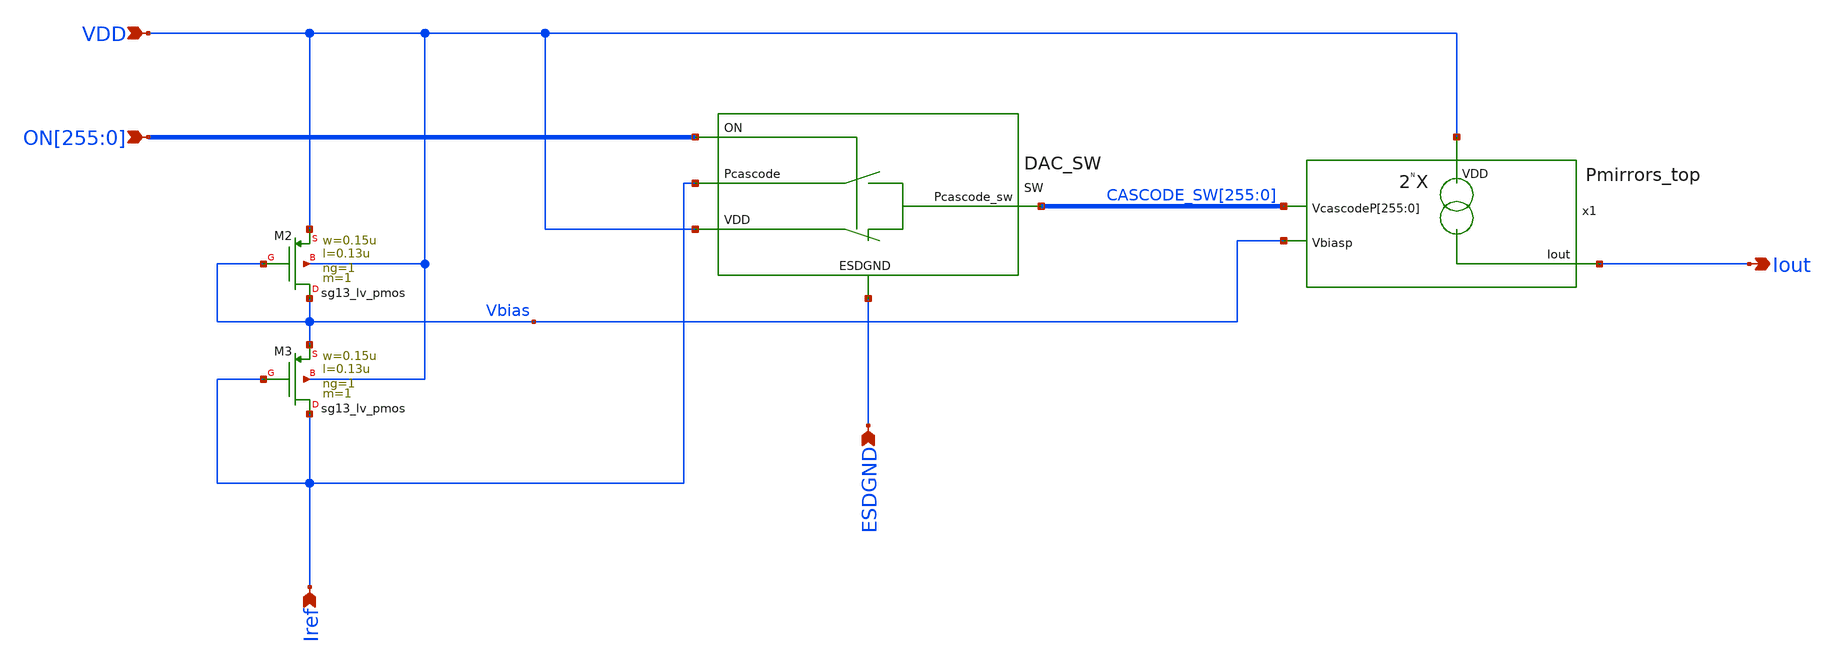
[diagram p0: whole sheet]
** sch_path: xschem/DAC_TOP.sch
**.subckt DAC_TOP VDD Iout ESDGND
*+ ON[255],ON[254],ON[253],ON[252],ON[251],ON[250],ON[249],ON[248],ON[247],ON[246],ON[245],ON[244],ON[243],ON[242],ON[241],ON[240],ON[239],ON[238],ON[237],ON[236],ON[235],ON[234],ON[233],ON[232],ON[231],ON[230],ON[229],ON[228],ON[227],ON[226],ON[225],ON[224],ON[223],ON[222],ON[221],ON[220],ON[219],ON[218],ON[217],ON[216],ON[215],ON[214],ON[213],ON[212],ON[211],ON[210],ON[209],ON[208],ON[207],ON[206],ON[205],ON[204],ON[203],ON[202],ON[201],ON[200],ON[199],ON[198],ON[197],ON[196],ON[195],ON[194],ON[193],ON[192],ON[191],ON[190],ON[189],ON[188],ON[187],ON[186],ON[185],ON[184],ON[183],ON[182],ON[181],ON[180],ON[179],ON[178],ON[177],ON[176],ON[175],ON[174],ON[173],ON[172],ON[171],ON[170],ON[169],ON[168],ON[167],ON[166],ON[165],ON[164],ON[163],ON[162],ON[161],ON[160],ON[159],ON[158],ON[157],ON[156],ON[155],ON[154],ON[153],ON[152],ON[151],ON[150],ON[149],ON[148],ON[147],ON[146],ON[145],ON[144],ON[143],ON[142],ON[141],ON[140],ON[139],ON[138],ON[137],ON[136],ON[135],ON[134],ON[133],ON[132],ON[131],ON[130],ON[129],ON[128],ON[127],ON[126],ON[125],ON[124],ON[123],ON[122],ON[121],ON[120],ON[119],ON[118],ON[117],ON[116],ON[115],ON[114],ON[113],ON[112],ON[111],ON[110],ON[109],ON[108],ON[107],ON[106],ON[105],ON[104],ON[103],ON[102],ON[101],ON[100],ON[99],ON[98],ON[97],ON[96],ON[95],ON[94],ON[93],ON[92],ON[91],ON[90],ON[89],ON[88],ON[87],ON[86],ON[85],ON[84],ON[83],ON[82],ON[81],ON[80],ON[79],ON[78],ON[77],ON[76],ON[75],ON[74],ON[73],ON[72],ON[71],ON[70],ON[69],ON[68],ON[67],ON[66],ON[65],ON[64],ON[63],ON[62],ON[61],ON[60],ON[59],ON[58],ON[57],ON[56],ON[55],ON[54],ON[53],ON[52],ON[51],ON[50],ON[49],ON[48],ON[47],ON[46],ON[45],ON[44],ON[43],ON[42],ON[41],ON[40],ON[39],ON[38],ON[37],ON[36],ON[35],ON[34],ON[33],ON[32],ON[31],ON[30],ON[29],ON[28],ON[27],ON[26],ON[25],ON[24],ON[23],ON[22],ON[21],ON[20],ON[19],ON[18],ON[17],ON[16],ON[15],ON[14],ON[13],ON[12],ON[11],ON[10],ON[9],ON[8],ON[7],ON[6],ON[5],ON[4],ON[3],ON[2],ON[1],ON[0] Iref
*.ipin VDD
*.opin Iout
*.ipin ESDGND
*.ipin
*+ ON[255],ON[254],ON[253],ON[252],ON[251],ON[250],ON[249],ON[248],ON[247],ON[246],ON[245],ON[244],ON[243],ON[242],ON[241],ON[240],ON[239],ON[238],ON[237],ON[236],ON[235],ON[234],ON[233],ON[232],ON[231],ON[230],ON[229],ON[228],ON[227],ON[226],ON[225],ON[224],ON[223],ON[222],ON[221],ON[220],ON[219],ON[218],ON[217],ON[216],ON[215],ON[214],ON[213],ON[212],ON[211],ON[210],ON[209],ON[208],ON[207],ON[206],ON[205],ON[204],ON[203],ON[202],ON[201],ON[200],ON[199],ON[198],ON[197],ON[196],ON[195],ON[194],ON[193],ON[192],ON[191],ON[190],ON[189],ON[188],ON[187],ON[186],ON[185],ON[184],ON[183],ON[182],ON[181],ON[180],ON[179],ON[178],ON[177],ON[176],ON[175],ON[174],ON[173],ON[172],ON[171],ON[170],ON[169],ON[168],ON[167],ON[166],ON[165],ON[164],ON[163],ON[162],ON[161],ON[160],ON[159],ON[158],ON[157],ON[156],ON[155],ON[154],ON[153],ON[152],ON[151],ON[150],ON[149],ON[148],ON[147],ON[146],ON[145],ON[144],ON[143],ON[142],ON[141],ON[140],ON[139],ON[138],ON[137],ON[136],ON[135],ON[134],ON[133],ON[132],ON[131],ON[130],ON[129],ON[128],ON[127],ON[126],ON[125],ON[124],ON[123],ON[122],ON[121],ON[120],ON[119],ON[118],ON[117],ON[116],ON[115],ON[114],ON[113],ON[112],ON[111],ON[110],ON[109],ON[108],ON[107],ON[106],ON[105],ON[104],ON[103],ON[102],ON[101],ON[100],ON[99],ON[98],ON[97],ON[96],ON[95],ON[94],ON[93],ON[92],ON[91],ON[90],ON[89],ON[88],ON[87],ON[86],ON[85],ON[84],ON[83],ON[82],ON[81],ON[80],ON[79],ON[78],ON[77],ON[76],ON[75],ON[74],ON[73],ON[72],ON[71],ON[70],ON[69],ON[68],ON[67],ON[66],ON[65],ON[64],ON[63],ON[62],ON[61],ON[60],ON[59],ON[58],ON[57],ON[56],ON[55],ON[54],ON[53],ON[52],ON[51],ON[50],ON[49],ON[48],ON[47],ON[46],ON[45],ON[44],ON[43],ON[42],ON[41],ON[40],ON[39],ON[38],ON[37],ON[36],ON[35],ON[34],ON[33],ON[32],ON[31],ON[30],ON[29],ON[28],ON[27],ON[26],ON[25],ON[24],ON[23],ON[22],ON[21],ON[20],ON[19],ON[18],ON[17],ON[16],ON[15],ON[14],ON[13],ON[12],ON[11],ON[10],ON[9],ON[8],ON[7],ON[6],ON[5],ON[4],ON[3],ON[2],ON[1],ON[0]
*.ipin Iref
x1 VDD Iout Vbias CASCODE_SW[255] CASCODE_SW[254] CASCODE_SW[253] CASCODE_SW[252] CASCODE_SW[251]
+ CASCODE_SW[250] CASCODE_SW[249] CASCODE_SW[248] CASCODE_SW[247] CASCODE_SW[246] CASCODE_SW[245] CASCODE_SW[244]
+ CASCODE_SW[243] CASCODE_SW[242] CASCODE_SW[241] CASCODE_SW[240] CASCODE_SW[239] CASCODE_SW[238] CASCODE_SW[237]
+ CASCODE_SW[236] CASCODE_SW[235] CASCODE_SW[234] CASCODE_SW[233] CASCODE_SW[232] CASCODE_SW[231] CASCODE_SW[230]
+ CASCODE_SW[229] CASCODE_SW[228] CASCODE_SW[227] CASCODE_SW[226] CASCODE_SW[225] CASCODE_SW[224] CASCODE_SW[223]
+ CASCODE_SW[222] CASCODE_SW[221] CASCODE_SW[220] CASCODE_SW[219] CASCODE_SW[218] CASCODE_SW[217] CASCODE_SW[216]
+ CASCODE_SW[215] CASCODE_SW[214] CASCODE_SW[213] CASCODE_SW[212] CASCODE_SW[211] CASCODE_SW[210] CASCODE_SW[209]
+ CASCODE_SW[208] CASCODE_SW[207] CASCODE_SW[206] CASCODE_SW[205] CASCODE_SW[204] CASCODE_SW[203] CASCODE_SW[202]
+ CASCODE_SW[201] CASCODE_SW[200] CASCODE_SW[199] CASCODE_SW[198] CASCODE_SW[197] CASCODE_SW[196] CASCODE_SW[195]
+ CASCODE_SW[194] CASCODE_SW[193] CASCODE_SW[192] CASCODE_SW[191] CASCODE_SW[190] CASCODE_SW[189] CASCODE_SW[188]
+ CASCODE_SW[187] CASCODE_SW[186] CASCODE_SW[185] CASCODE_SW[184] CASCODE_SW[183] CASCODE_SW[182] CASCODE_SW[181]
+ CASCODE_SW[180] CASCODE_SW[179] CASCODE_SW[178] CASCODE_SW[177] CASCODE_SW[176] CASCODE_SW[175] CASCODE_SW[174]
+ CASCODE_SW[173] CASCODE_SW[172] CASCODE_SW[171] CASCODE_SW[170] CASCODE_SW[169] CASCODE_SW[168] CASCODE_SW[167]
+ CASCODE_SW[166] CASCODE_SW[165] CASCODE_SW[164] CASCODE_SW[163] CASCODE_SW[162] CASCODE_SW[161] CASCODE_SW[160]
+ CASCODE_SW[159] CASCODE_SW[158] CASCODE_SW[157] CASCODE_SW[156] CASCODE_SW[155] CASCODE_SW[154] CASCODE_SW[153]
+ CASCODE_SW[152] CASCODE_SW[151] CASCODE_SW[150] CASCODE_SW[149] CASCODE_SW[148] CASCODE_SW[147] CASCODE_SW[146]
+ CASCODE_SW[145] CASCODE_SW[144] CASCODE_SW[143] CASCODE_SW[142] CASCODE_SW[141] CASCODE_SW[140] CASCODE_SW[139]
+ CASCODE_SW[138] CASCODE_SW[137] CASCODE_SW[136] CASCODE_SW[135] CASCODE_SW[134] CASCODE_SW[133] CASCODE_SW[132]
+ CASCODE_SW[131] CASCODE_SW[130] CASCODE_SW[129] CASCODE_SW[128] CASCODE_SW[127] CASCODE_SW[126] CASCODE_SW[125]
+ CASCODE_SW[124] CASCODE_SW[123] CASCODE_SW[122] CASCODE_SW[121] CASCODE_SW[120] CASCODE_SW[119] CASCODE_SW[118]
+ CASCODE_SW[117] CASCODE_SW[116] CASCODE_SW[115] CASCODE_SW[114] CASCODE_SW[113] CASCODE_SW[112] CASCODE_SW[111]
+ CASCODE_SW[110] CASCODE_SW[109] CASCODE_SW[108] CASCODE_SW[107] CASCODE_SW[106] CASCODE_SW[105] CASCODE_SW[104]
+ CASCODE_SW[103] CASCODE_SW[102] CASCODE_SW[101] CASCODE_SW[100] CASCODE_SW[99] CASCODE_SW[98] CASCODE_SW[97]
+ CASCODE_SW[96] CASCODE_SW[95] CASCODE_SW[94] CASCODE_SW[93] CASCODE_SW[92] CASCODE_SW[91] CASCODE_SW[90]
+ CASCODE_SW[89] CASCODE_SW[88] CASCODE_SW[87] CASCODE_SW[86] CASCODE_SW[85] CASCODE_SW[84] CASCODE_SW[83]
+ CASCODE_SW[82] CASCODE_SW[81] CASCODE_SW[80] CASCODE_SW[79] CASCODE_SW[78] CASCODE_SW[77] CASCODE_SW[76]
+ CASCODE_SW[75] CASCODE_SW[74] CASCODE_SW[73] CASCODE_SW[72] CASCODE_SW[71] CASCODE_SW[70] CASCODE_SW[69]
+ CASCODE_SW[68] CASCODE_SW[67] CASCODE_SW[66] CASCODE_SW[65] CASCODE_SW[64] CASCODE_SW[63] CASCODE_SW[62]
+ CASCODE_SW[61] CASCODE_SW[60] CASCODE_SW[59] CASCODE_SW[58] CASCODE_SW[57] CASCODE_SW[56] CASCODE_SW[55]
+ CASCODE_SW[54] CASCODE_SW[53] CASCODE_SW[52] CASCODE_SW[51] CASCODE_SW[50] CASCODE_SW[49] CASCODE_SW[48]
+ CASCODE_SW[47] CASCODE_SW[46] CASCODE_SW[45] CASCODE_SW[44] CASCODE_SW[43] CASCODE_SW[42] CASCODE_SW[41]
+ CASCODE_SW[40] CASCODE_SW[39] CASCODE_SW[38] CASCODE_SW[37] CASCODE_SW[36] CASCODE_SW[35] CASCODE_SW[34]
+ CASCODE_SW[33] CASCODE_SW[32] CASCODE_SW[31] CASCODE_SW[30] CASCODE_SW[29] CASCODE_SW[28] CASCODE_SW[27]
+ CASCODE_SW[26] CASCODE_SW[25] CASCODE_SW[24] CASCODE_SW[23] CASCODE_SW[22] CASCODE_SW[21] CASCODE_SW[20]
+ CASCODE_SW[19] CASCODE_SW[18] CASCODE_SW[17] CASCODE_SW[16] CASCODE_SW[15] CASCODE_SW[14] CASCODE_SW[13]
+ CASCODE_SW[12] CASCODE_SW[11] CASCODE_SW[10] CASCODE_SW[9] CASCODE_SW[8] CASCODE_SW[7] CASCODE_SW[6] CASCODE_SW[5]
+ CASCODE_SW[4] CASCODE_SW[3] CASCODE_SW[2] CASCODE_SW[1] CASCODE_SW[0] Pmirrors_top
SW VDD ON[255] CASCODE_SW[255] Iref ESDGND DAC_SW
XM2 Vbias Vbias VDD VDD sg13_lv_pmos w=0.15u l=0.13u ng=1 m=1 mm_ok=1
XM3 Iref Iref Vbias VDD sg13_lv_pmos w=0.15u l=0.13u ng=1 m=1 mm_ok=1
**.ends

* expanding   symbol:  /home/user/PUDDING/schematic/Pmirrors_top.sym # of pins=4
** sym_path: /home/user/PUDDING/schematic/Pmirrors_top.sym
** sch_path: /home/user/PUDDING/schematic/Pmirrors_top.sch
.subckt Pmirrors_top VDD Iout Vbiasp VcascodeP[255] VcascodeP[254] VcascodeP[253] VcascodeP[252]
+ VcascodeP[251] VcascodeP[250] VcascodeP[249] VcascodeP[248] VcascodeP[247] VcascodeP[246] VcascodeP[245]
+ VcascodeP[244] VcascodeP[243] VcascodeP[242] VcascodeP[241] VcascodeP[240] VcascodeP[239] VcascodeP[238]
+ VcascodeP[237] VcascodeP[236] VcascodeP[235] VcascodeP[234] VcascodeP[233] VcascodeP[232] VcascodeP[231]
+ VcascodeP[230] VcascodeP[229] VcascodeP[228] VcascodeP[227] VcascodeP[226] VcascodeP[225] VcascodeP[224]
+ VcascodeP[223] VcascodeP[222] VcascodeP[221] VcascodeP[220] VcascodeP[219] VcascodeP[218] VcascodeP[217]
+ VcascodeP[216] VcascodeP[215] VcascodeP[214] VcascodeP[213] VcascodeP[212] VcascodeP[211] VcascodeP[210]
+ VcascodeP[209] VcascodeP[208] VcascodeP[207] VcascodeP[206] VcascodeP[205] VcascodeP[204] VcascodeP[203]
+ VcascodeP[202] VcascodeP[201] VcascodeP[200] VcascodeP[199] VcascodeP[198] VcascodeP[197] VcascodeP[196]
+ VcascodeP[195] VcascodeP[194] VcascodeP[193] VcascodeP[192] VcascodeP[191] VcascodeP[190] VcascodeP[189]
+ VcascodeP[188] VcascodeP[187] VcascodeP[186] VcascodeP[185] VcascodeP[184] VcascodeP[183] VcascodeP[182]
+ VcascodeP[181] VcascodeP[180] VcascodeP[179] VcascodeP[178] VcascodeP[177] VcascodeP[176] VcascodeP[175]
+ VcascodeP[174] VcascodeP[173] VcascodeP[172] VcascodeP[171] VcascodeP[170] VcascodeP[169] VcascodeP[168]
+ VcascodeP[167] VcascodeP[166] VcascodeP[165] VcascodeP[164] VcascodeP[163] VcascodeP[162] VcascodeP[161]
+ VcascodeP[160] VcascodeP[159] VcascodeP[158] VcascodeP[157] VcascodeP[156] VcascodeP[155] VcascodeP[154]
+ VcascodeP[153] VcascodeP[152] VcascodeP[151] VcascodeP[150] VcascodeP[149] VcascodeP[148] VcascodeP[147]
+ VcascodeP[146] VcascodeP[145] VcascodeP[144] VcascodeP[143] VcascodeP[142] VcascodeP[141] VcascodeP[140]
+ VcascodeP[139] VcascodeP[138] VcascodeP[137] VcascodeP[136] VcascodeP[135] VcascodeP[134] VcascodeP[133]
+ VcascodeP[132] VcascodeP[131] VcascodeP[130] VcascodeP[129] VcascodeP[128] VcascodeP[127] VcascodeP[126]
+ VcascodeP[125] VcascodeP[124] VcascodeP[123] VcascodeP[122] VcascodeP[121] VcascodeP[120] VcascodeP[119]
+ VcascodeP[118] VcascodeP[117] VcascodeP[116] VcascodeP[115] VcascodeP[114] VcascodeP[113] VcascodeP[112]
+ VcascodeP[111] VcascodeP[110] VcascodeP[109] VcascodeP[108] VcascodeP[107] VcascodeP[106] VcascodeP[105]
+ VcascodeP[104] VcascodeP[103] VcascodeP[102] VcascodeP[101] VcascodeP[100] VcascodeP[99] VcascodeP[98]
+ VcascodeP[97] VcascodeP[96] VcascodeP[95] VcascodeP[94] VcascodeP[93] VcascodeP[92] VcascodeP[91] VcascodeP[90]
+ VcascodeP[89] VcascodeP[88] VcascodeP[87] VcascodeP[86] VcascodeP[85] VcascodeP[84] VcascodeP[83] VcascodeP[82]
+ VcascodeP[81] VcascodeP[80] VcascodeP[79] VcascodeP[78] VcascodeP[77] VcascodeP[76] VcascodeP[75] VcascodeP[74]
+ VcascodeP[73] VcascodeP[72] VcascodeP[71] VcascodeP[70] VcascodeP[69] VcascodeP[68] VcascodeP[67] VcascodeP[66]
+ VcascodeP[65] VcascodeP[64] VcascodeP[63] VcascodeP[62] VcascodeP[61] VcascodeP[60] VcascodeP[59] VcascodeP[58]
+ VcascodeP[57] VcascodeP[56] VcascodeP[55] VcascodeP[54] VcascodeP[53] VcascodeP[52] VcascodeP[51] VcascodeP[50]
+ VcascodeP[49] VcascodeP[48] VcascodeP[47] VcascodeP[46] VcascodeP[45] VcascodeP[44] VcascodeP[43] VcascodeP[42]
+ VcascodeP[41] VcascodeP[40] VcascodeP[39] VcascodeP[38] VcascodeP[37] VcascodeP[36] VcascodeP[35] VcascodeP[34]
+ VcascodeP[33] VcascodeP[32] VcascodeP[31] VcascodeP[30] VcascodeP[29] VcascodeP[28] VcascodeP[27] VcascodeP[26]
+ VcascodeP[25] VcascodeP[24] VcascodeP[23] VcascodeP[22] VcascodeP[21] VcascodeP[20] VcascodeP[19] VcascodeP[18]
+ VcascodeP[17] VcascodeP[16] VcascodeP[15] VcascodeP[14] VcascodeP[13] VcascodeP[12] VcascodeP[11] VcascodeP[10]
+ VcascodeP[9] VcascodeP[8] VcascodeP[7] VcascodeP[6] VcascodeP[5] VcascodeP[4] VcascodeP[3] VcascodeP[2]
+ VcascodeP[1] VcascodeP[0]
*.ipin Vbiasp
*.ipin VDD
*.ipin
*+ VcascodeP[255],VcascodeP[254],VcascodeP[253],VcascodeP[252],VcascodeP[251],VcascodeP[250],VcascodeP[249],VcascodeP[248],VcascodeP[247],VcascodeP[246],VcascodeP[245],VcascodeP[244],VcascodeP[243],VcascodeP[242],VcascodeP[241],VcascodeP[240],VcascodeP[239],VcascodeP[238],VcascodeP[237],VcascodeP[236],VcascodeP[235],VcascodeP[234],VcascodeP[233],VcascodeP[232],VcascodeP[231],VcascodeP[230],VcascodeP[229],VcascodeP[228],VcascodeP[227],VcascodeP[226],VcascodeP[225],VcascodeP[224],VcascodeP[223],VcascodeP[222],VcascodeP[221],VcascodeP[220],VcascodeP[219],VcascodeP[218],VcascodeP[217],VcascodeP[216],VcascodeP[215],VcascodeP[214],VcascodeP[213],VcascodeP[212],VcascodeP[211],VcascodeP[210],VcascodeP[209],VcascodeP[208],VcascodeP[207],VcascodeP[206],VcascodeP[205],VcascodeP[204],VcascodeP[203],VcascodeP[202],VcascodeP[201],VcascodeP[200],VcascodeP[199],VcascodeP[198],VcascodeP[197],VcascodeP[196],VcascodeP[195],VcascodeP[194],VcascodeP[193],VcascodeP[192],VcascodeP[191],VcascodeP[190],VcascodeP[189],VcascodeP[188],VcascodeP[187],VcascodeP[186],VcascodeP[185],VcascodeP[184],VcascodeP[183],VcascodeP[182],VcascodeP[181],VcascodeP[180],VcascodeP[179],VcascodeP[178],VcascodeP[177],VcascodeP[176],VcascodeP[175],VcascodeP[174],VcascodeP[173],VcascodeP[172],VcascodeP[171],VcascodeP[170],VcascodeP[169],VcascodeP[168],VcascodeP[167],VcascodeP[166],VcascodeP[165],VcascodeP[164],VcascodeP[163],VcascodeP[162],VcascodeP[161],VcascodeP[160],VcascodeP[159],VcascodeP[158],VcascodeP[157],VcascodeP[156],VcascodeP[155],VcascodeP[154],VcascodeP[153],VcascodeP[152],VcascodeP[151],VcascodeP[150],VcascodeP[149],VcascodeP[148],VcascodeP[147],VcascodeP[146],VcascodeP[145],VcascodeP[144],VcascodeP[143],VcascodeP[142],VcascodeP[141],VcascodeP[140],VcascodeP[139],VcascodeP[138],VcascodeP[137],VcascodeP[136],VcascodeP[135],VcascodeP[134],VcascodeP[133],VcascodeP[132],VcascodeP[131],VcascodeP[130],VcascodeP[129],VcascodeP[128],VcascodeP[127],VcascodeP[126],VcascodeP[125],VcascodeP[124],VcascodeP[123],VcascodeP[122],VcascodeP[121],VcascodeP[120],VcascodeP[119],VcascodeP[118],VcascodeP[117],VcascodeP[116],VcascodeP[115],VcascodeP[114],VcascodeP[113],VcascodeP[112],VcascodeP[111],VcascodeP[110],VcascodeP[109],VcascodeP[108],VcascodeP[107],VcascodeP[106],VcascodeP[105],VcascodeP[104],VcascodeP[103],VcascodeP[102],VcascodeP[101],VcascodeP[100],VcascodeP[99],VcascodeP[98],VcascodeP[97],VcascodeP[96],VcascodeP[95],VcascodeP[94],VcascodeP[93],VcascodeP[92],VcascodeP[91],VcascodeP[90],VcascodeP[89],VcascodeP[88],VcascodeP[87],VcascodeP[86],VcascodeP[85],VcascodeP[84],VcascodeP[83],VcascodeP[82],VcascodeP[81],VcascodeP[80],VcascodeP[79],VcascodeP[78],VcascodeP[77],VcascodeP[76],VcascodeP[75],VcascodeP[74],VcascodeP[73],VcascodeP[72],VcascodeP[71],VcascodeP[70],VcascodeP[69],VcascodeP[68],VcascodeP[67],VcascodeP[66],VcascodeP[65],VcascodeP[64],VcascodeP[63],VcascodeP[62],VcascodeP[61],VcascodeP[60],VcascodeP[59],VcascodeP[58],VcascodeP[57],VcascodeP[56],VcascodeP[55],VcascodeP[54],VcascodeP[53],VcascodeP[52],VcascodeP[51],VcascodeP[50],VcascodeP[49],VcascodeP[48],VcascodeP[47],VcascodeP[46],VcascodeP[45],VcascodeP[44],VcascodeP[43],VcascodeP[42],VcascodeP[41],VcascodeP[40],VcascodeP[39],VcascodeP[38],VcascodeP[37],VcascodeP[36],VcascodeP[35],VcascodeP[34],VcascodeP[33],VcascodeP[32],VcascodeP[31],VcascodeP[30],VcascodeP[29],VcascodeP[28],VcascodeP[27],VcascodeP[26],VcascodeP[25],VcascodeP[24],VcascodeP[23],VcascodeP[22],VcascodeP[21],VcascodeP[20],VcascodeP[19],VcascodeP[18],VcascodeP[17],VcascodeP[16],VcascodeP[15],VcascodeP[14],VcascodeP[13],VcascodeP[12],VcascodeP[11],VcascodeP[10],VcascodeP[9],VcascodeP[8],VcascodeP[7],VcascodeP[6],VcascodeP[5],VcascodeP[4],VcascodeP[3],VcascodeP[2],VcascodeP[1],VcascodeP[0]
*.opin Iout
XI_MIRROR[255] VDD Vbiasp VcascodeP[255] Iout Pmirror_StdCell
XI_MIRROR[254] VDD Vbiasp VcascodeP[254] Iout Pmirror_StdCell
XI_MIRROR[253] VDD Vbiasp VcascodeP[253] Iout Pmirror_StdCell
XI_MIRROR[252] VDD Vbiasp VcascodeP[252] Iout Pmirror_StdCell
XI_MIRROR[251] VDD Vbiasp VcascodeP[251] Iout Pmirror_StdCell
XI_MIRROR[250] VDD Vbiasp VcascodeP[250] Iout Pmirror_StdCell
XI_MIRROR[249] VDD Vbiasp VcascodeP[249] Iout Pmirror_StdCell
XI_MIRROR[248] VDD Vbiasp VcascodeP[248] Iout Pmirror_StdCell
XI_MIRROR[247] VDD Vbiasp VcascodeP[247] Iout Pmirror_StdCell
XI_MIRROR[246] VDD Vbiasp VcascodeP[246] Iout Pmirror_StdCell
XI_MIRROR[245] VDD Vbiasp VcascodeP[245] Iout Pmirror_StdCell
XI_MIRROR[244] VDD Vbiasp VcascodeP[244] Iout Pmirror_StdCell
XI_MIRROR[243] VDD Vbiasp VcascodeP[243] Iout Pmirror_StdCell
XI_MIRROR[242] VDD Vbiasp VcascodeP[242] Iout Pmirror_StdCell
XI_MIRROR[241] VDD Vbiasp VcascodeP[241] Iout Pmirror_StdCell
XI_MIRROR[240] VDD Vbiasp VcascodeP[240] Iout Pmirror_StdCell
XI_MIRROR[239] VDD Vbiasp VcascodeP[239] Iout Pmirror_StdCell
XI_MIRROR[238] VDD Vbiasp VcascodeP[238] Iout Pmirror_StdCell
XI_MIRROR[237] VDD Vbiasp VcascodeP[237] Iout Pmirror_StdCell
XI_MIRROR[236] VDD Vbiasp VcascodeP[236] Iout Pmirror_StdCell
XI_MIRROR[235] VDD Vbiasp VcascodeP[235] Iout Pmirror_StdCell
XI_MIRROR[234] VDD Vbiasp VcascodeP[234] Iout Pmirror_StdCell
XI_MIRROR[233] VDD Vbiasp VcascodeP[233] Iout Pmirror_StdCell
XI_MIRROR[232] VDD Vbiasp VcascodeP[232] Iout Pmirror_StdCell
XI_MIRROR[231] VDD Vbiasp VcascodeP[231] Iout Pmirror_StdCell
XI_MIRROR[230] VDD Vbiasp VcascodeP[230] Iout Pmirror_StdCell
XI_MIRROR[229] VDD Vbiasp VcascodeP[229] Iout Pmirror_StdCell
XI_MIRROR[228] VDD Vbiasp VcascodeP[228] Iout Pmirror_StdCell
XI_MIRROR[227] VDD Vbiasp VcascodeP[227] Iout Pmirror_StdCell
XI_MIRROR[226] VDD Vbiasp VcascodeP[226] Iout Pmirror_StdCell
XI_MIRROR[225] VDD Vbiasp VcascodeP[225] Iout Pmirror_StdCell
XI_MIRROR[224] VDD Vbiasp VcascodeP[224] Iout Pmirror_StdCell
XI_MIRROR[223] VDD Vbiasp VcascodeP[223] Iout Pmirror_StdCell
XI_MIRROR[222] VDD Vbiasp VcascodeP[222] Iout Pmirror_StdCell
XI_MIRROR[221] VDD Vbiasp VcascodeP[221] Iout Pmirror_StdCell
XI_MIRROR[220] VDD Vbiasp VcascodeP[220] Iout Pmirror_StdCell
XI_MIRROR[219] VDD Vbiasp VcascodeP[219] Iout Pmirror_StdCell
XI_MIRROR[218] VDD Vbiasp VcascodeP[218] Iout Pmirror_StdCell
XI_MIRROR[217] VDD Vbiasp VcascodeP[217] Iout Pmirror_StdCell
XI_MIRROR[216] VDD Vbiasp VcascodeP[216] Iout Pmirror_StdCell
XI_MIRROR[215] VDD Vbiasp VcascodeP[215] Iout Pmirror_StdCell
XI_MIRROR[214] VDD Vbiasp VcascodeP[214] Iout Pmirror_StdCell
XI_MIRROR[213] VDD Vbiasp VcascodeP[213] Iout Pmirror_StdCell
XI_MIRROR[212] VDD Vbiasp VcascodeP[212] Iout Pmirror_StdCell
XI_MIRROR[211] VDD Vbiasp VcascodeP[211] Iout Pmirror_StdCell
XI_MIRROR[210] VDD Vbiasp VcascodeP[210] Iout Pmirror_StdCell
XI_MIRROR[209] VDD Vbiasp VcascodeP[209] Iout Pmirror_StdCell
XI_MIRROR[208] VDD Vbiasp VcascodeP[208] Iout Pmirror_StdCell
XI_MIRROR[207] VDD Vbiasp VcascodeP[207] Iout Pmirror_StdCell
XI_MIRROR[206] VDD Vbiasp VcascodeP[206] Iout Pmirror_StdCell
XI_MIRROR[205] VDD Vbiasp VcascodeP[205] Iout Pmirror_StdCell
XI_MIRROR[204] VDD Vbiasp VcascodeP[204] Iout Pmirror_StdCell
XI_MIRROR[203] VDD Vbiasp VcascodeP[203] Iout Pmirror_StdCell
XI_MIRROR[202] VDD Vbiasp VcascodeP[202] Iout Pmirror_StdCell
XI_MIRROR[201] VDD Vbiasp VcascodeP[201] Iout Pmirror_StdCell
XI_MIRROR[200] VDD Vbiasp VcascodeP[200] Iout Pmirror_StdCell
XI_MIRROR[199] VDD Vbiasp VcascodeP[199] Iout Pmirror_StdCell
XI_MIRROR[198] VDD Vbiasp VcascodeP[198] Iout Pmirror_StdCell
XI_MIRROR[197] VDD Vbiasp VcascodeP[197] Iout Pmirror_StdCell
XI_MIRROR[196] VDD Vbiasp VcascodeP[196] Iout Pmirror_StdCell
XI_MIRROR[195] VDD Vbiasp VcascodeP[195] Iout Pmirror_StdCell
XI_MIRROR[194] VDD Vbiasp VcascodeP[194] Iout Pmirror_StdCell
XI_MIRROR[193] VDD Vbiasp VcascodeP[193] Iout Pmirror_StdCell
XI_MIRROR[192] VDD Vbiasp VcascodeP[192] Iout Pmirror_StdCell
XI_MIRROR[191] VDD Vbiasp VcascodeP[191] Iout Pmirror_StdCell
XI_MIRROR[190] VDD Vbiasp VcascodeP[190] Iout Pmirror_StdCell
XI_MIRROR[189] VDD Vbiasp VcascodeP[189] Iout Pmirror_StdCell
XI_MIRROR[188] VDD Vbiasp VcascodeP[188] Iout Pmirror_StdCell
XI_MIRROR[187] VDD Vbiasp VcascodeP[187] Iout Pmirror_StdCell
XI_MIRROR[186] VDD Vbiasp VcascodeP[186] Iout Pmirror_StdCell
XI_MIRROR[185] VDD Vbiasp VcascodeP[185] Iout Pmirror_StdCell
XI_MIRROR[184] VDD Vbiasp VcascodeP[184] Iout Pmirror_StdCell
XI_MIRROR[183] VDD Vbiasp VcascodeP[183] Iout Pmirror_StdCell
XI_MIRROR[182] VDD Vbiasp VcascodeP[182] Iout Pmirror_StdCell
XI_MIRROR[181] VDD Vbiasp VcascodeP[181] Iout Pmirror_StdCell
XI_MIRROR[180] VDD Vbiasp VcascodeP[180] Iout Pmirror_StdCell
XI_MIRROR[179] VDD Vbiasp VcascodeP[179] Iout Pmirror_StdCell
XI_MIRROR[178] VDD Vbiasp VcascodeP[178] Iout Pmirror_StdCell
XI_MIRROR[177] VDD Vbiasp VcascodeP[177] Iout Pmirror_StdCell
XI_MIRROR[176] VDD Vbiasp VcascodeP[176] Iout Pmirror_StdCell
XI_MIRROR[175] VDD Vbiasp VcascodeP[175] Iout Pmirror_StdCell
XI_MIRROR[174] VDD Vbiasp VcascodeP[174] Iout Pmirror_StdCell
XI_MIRROR[173] VDD Vbiasp VcascodeP[173] Iout Pmirror_StdCell
XI_MIRROR[172] VDD Vbiasp VcascodeP[172] Iout Pmirror_StdCell
XI_MIRROR[171] VDD Vbiasp VcascodeP[171] Iout Pmirror_StdCell
XI_MIRROR[170] VDD Vbiasp VcascodeP[170] Iout Pmirror_StdCell
XI_MIRROR[169] VDD Vbiasp VcascodeP[169] Iout Pmirror_StdCell
XI_MIRROR[168] VDD Vbiasp VcascodeP[168] Iout Pmirror_StdCell
XI_MIRROR[167] VDD Vbiasp VcascodeP[167] Iout Pmirror_StdCell
XI_MIRROR[166] VDD Vbiasp VcascodeP[166] Iout Pmirror_StdCell
XI_MIRROR[165] VDD Vbiasp VcascodeP[165] Iout Pmirror_StdCell
XI_MIRROR[164] VDD Vbiasp VcascodeP[164] Iout Pmirror_StdCell
XI_MIRROR[163] VDD Vbiasp VcascodeP[163] Iout Pmirror_StdCell
XI_MIRROR[162] VDD Vbiasp VcascodeP[162] Iout Pmirror_StdCell
XI_MIRROR[161] VDD Vbiasp VcascodeP[161] Iout Pmirror_StdCell
XI_MIRROR[160] VDD Vbiasp VcascodeP[160] Iout Pmirror_StdCell
XI_MIRROR[159] VDD Vbiasp VcascodeP[159] Iout Pmirror_StdCell
XI_MIRROR[158] VDD Vbiasp VcascodeP[158] Iout Pmirror_StdCell
XI_MIRROR[157] VDD Vbiasp VcascodeP[157] Iout Pmirror_StdCell
XI_MIRROR[156] VDD Vbiasp VcascodeP[156] Iout Pmirror_StdCell
XI_MIRROR[155] VDD Vbiasp VcascodeP[155] Iout Pmirror_StdCell
XI_MIRROR[154] VDD Vbiasp VcascodeP[154] Iout Pmirror_StdCell
XI_MIRROR[153] VDD Vbiasp VcascodeP[153] Iout Pmirror_StdCell
XI_MIRROR[152] VDD Vbiasp VcascodeP[152] Iout Pmirror_StdCell
XI_MIRROR[151] VDD Vbiasp VcascodeP[151] Iout Pmirror_StdCell
XI_MIRROR[150] VDD Vbiasp VcascodeP[150] Iout Pmirror_StdCell
XI_MIRROR[149] VDD Vbiasp VcascodeP[149] Iout Pmirror_StdCell
XI_MIRROR[148] VDD Vbiasp VcascodeP[148] Iout Pmirror_StdCell
XI_MIRROR[147] VDD Vbiasp VcascodeP[147] Iout Pmirror_StdCell
XI_MIRROR[146] VDD Vbiasp VcascodeP[146] Iout Pmirror_StdCell
XI_MIRROR[145] VDD Vbiasp VcascodeP[145] Iout Pmirror_StdCell
XI_MIRROR[144] VDD Vbiasp VcascodeP[144] Iout Pmirror_StdCell
XI_MIRROR[143] VDD Vbiasp VcascodeP[143] Iout Pmirror_StdCell
XI_MIRROR[142] VDD Vbiasp VcascodeP[142] Iout Pmirror_StdCell
XI_MIRROR[141] VDD Vbiasp VcascodeP[141] Iout Pmirror_StdCell
XI_MIRROR[140] VDD Vbiasp VcascodeP[140] Iout Pmirror_StdCell
XI_MIRROR[139] VDD Vbiasp VcascodeP[139] Iout Pmirror_StdCell
XI_MIRROR[138] VDD Vbiasp VcascodeP[138] Iout Pmirror_StdCell
XI_MIRROR[137] VDD Vbiasp VcascodeP[137] Iout Pmirror_StdCell
XI_MIRROR[136] VDD Vbiasp VcascodeP[136] Iout Pmirror_StdCell
XI_MIRROR[135] VDD Vbiasp VcascodeP[135] Iout Pmirror_StdCell
XI_MIRROR[134] VDD Vbiasp VcascodeP[134] Iout Pmirror_StdCell
XI_MIRROR[133] VDD Vbiasp VcascodeP[133] Iout Pmirror_StdCell
XI_MIRROR[132] VDD Vbiasp VcascodeP[132] Iout Pmirror_StdCell
XI_MIRROR[131] VDD Vbiasp VcascodeP[131] Iout Pmirror_StdCell
XI_MIRROR[130] VDD Vbiasp VcascodeP[130] Iout Pmirror_StdCell
XI_MIRROR[129] VDD Vbiasp VcascodeP[129] Iout Pmirror_StdCell
XI_MIRROR[128] VDD Vbiasp VcascodeP[128] Iout Pmirror_StdCell
XI_MIRROR[127] VDD Vbiasp VcascodeP[127] Iout Pmirror_StdCell
XI_MIRROR[126] VDD Vbiasp VcascodeP[126] Iout Pmirror_StdCell
XI_MIRROR[125] VDD Vbiasp VcascodeP[125] Iout Pmirror_StdCell
XI_MIRROR[124] VDD Vbiasp VcascodeP[124] Iout Pmirror_StdCell
XI_MIRROR[123] VDD Vbiasp VcascodeP[123] Iout Pmirror_StdCell
XI_MIRROR[122] VDD Vbiasp VcascodeP[122] Iout Pmirror_StdCell
XI_MIRROR[121] VDD Vbiasp VcascodeP[121] Iout Pmirror_StdCell
XI_MIRROR[120] VDD Vbiasp VcascodeP[120] Iout Pmirror_StdCell
XI_MIRROR[119] VDD Vbiasp VcascodeP[119] Iout Pmirror_StdCell
XI_MIRROR[118] VDD Vbiasp VcascodeP[118] Iout Pmirror_StdCell
XI_MIRROR[117] VDD Vbiasp VcascodeP[117] Iout Pmirror_StdCell
XI_MIRROR[116] VDD Vbiasp VcascodeP[116] Iout Pmirror_StdCell
XI_MIRROR[115] VDD Vbiasp VcascodeP[115] Iout Pmirror_StdCell
XI_MIRROR[114] VDD Vbiasp VcascodeP[114] Iout Pmirror_StdCell
XI_MIRROR[113] VDD Vbiasp VcascodeP[113] Iout Pmirror_StdCell
XI_MIRROR[112] VDD Vbiasp VcascodeP[112] Iout Pmirror_StdCell
XI_MIRROR[111] VDD Vbiasp VcascodeP[111] Iout Pmirror_StdCell
XI_MIRROR[110] VDD Vbiasp VcascodeP[110] Iout Pmirror_StdCell
XI_MIRROR[109] VDD Vbiasp VcascodeP[109] Iout Pmirror_StdCell
XI_MIRROR[108] VDD Vbiasp VcascodeP[108] Iout Pmirror_StdCell
XI_MIRROR[107] VDD Vbiasp VcascodeP[107] Iout Pmirror_StdCell
XI_MIRROR[106] VDD Vbiasp VcascodeP[106] Iout Pmirror_StdCell
XI_MIRROR[105] VDD Vbiasp VcascodeP[105] Iout Pmirror_StdCell
XI_MIRROR[104] VDD Vbiasp VcascodeP[104] Iout Pmirror_StdCell
XI_MIRROR[103] VDD Vbiasp VcascodeP[103] Iout Pmirror_StdCell
XI_MIRROR[102] VDD Vbiasp VcascodeP[102] Iout Pmirror_StdCell
XI_MIRROR[101] VDD Vbiasp VcascodeP[101] Iout Pmirror_StdCell
XI_MIRROR[100] VDD Vbiasp VcascodeP[100] Iout Pmirror_StdCell
XI_MIRROR[99] VDD Vbiasp VcascodeP[99] Iout Pmirror_StdCell
XI_MIRROR[98] VDD Vbiasp VcascodeP[98] Iout Pmirror_StdCell
XI_MIRROR[97] VDD Vbiasp VcascodeP[97] Iout Pmirror_StdCell
XI_MIRROR[96] VDD Vbiasp VcascodeP[96] Iout Pmirror_StdCell
XI_MIRROR[95] VDD Vbiasp VcascodeP[95] Iout Pmirror_StdCell
XI_MIRROR[94] VDD Vbiasp VcascodeP[94] Iout Pmirror_StdCell
XI_MIRROR[93] VDD Vbiasp VcascodeP[93] Iout Pmirror_StdCell
XI_MIRROR[92] VDD Vbiasp VcascodeP[92] Iout Pmirror_StdCell
XI_MIRROR[91] VDD Vbiasp VcascodeP[91] Iout Pmirror_StdCell
XI_MIRROR[90] VDD Vbiasp VcascodeP[90] Iout Pmirror_StdCell
XI_MIRROR[89] VDD Vbiasp VcascodeP[89] Iout Pmirror_StdCell
XI_MIRROR[88] VDD Vbiasp VcascodeP[88] Iout Pmirror_StdCell
XI_MIRROR[87] VDD Vbiasp VcascodeP[87] Iout Pmirror_StdCell
XI_MIRROR[86] VDD Vbiasp VcascodeP[86] Iout Pmirror_StdCell
XI_MIRROR[85] VDD Vbiasp VcascodeP[85] Iout Pmirror_StdCell
XI_MIRROR[84] VDD Vbiasp VcascodeP[84] Iout Pmirror_StdCell
XI_MIRROR[83] VDD Vbiasp VcascodeP[83] Iout Pmirror_StdCell
XI_MIRROR[82] VDD Vbiasp VcascodeP[82] Iout Pmirror_StdCell
XI_MIRROR[81] VDD Vbiasp VcascodeP[81] Iout Pmirror_StdCell
XI_MIRROR[80] VDD Vbiasp VcascodeP[80] Iout Pmirror_StdCell
XI_MIRROR[79] VDD Vbiasp VcascodeP[79] Iout Pmirror_StdCell
XI_MIRROR[78] VDD Vbiasp VcascodeP[78] Iout Pmirror_StdCell
XI_MIRROR[77] VDD Vbiasp VcascodeP[77] Iout Pmirror_StdCell
XI_MIRROR[76] VDD Vbiasp VcascodeP[76] Iout Pmirror_StdCell
XI_MIRROR[75] VDD Vbiasp VcascodeP[75] Iout Pmirror_StdCell
XI_MIRROR[74] VDD Vbiasp VcascodeP[74] Iout Pmirror_StdCell
XI_MIRROR[73] VDD Vbiasp VcascodeP[73] Iout Pmirror_StdCell
XI_MIRROR[72] VDD Vbiasp VcascodeP[72] Iout Pmirror_StdCell
XI_MIRROR[71] VDD Vbiasp VcascodeP[71] Iout Pmirror_StdCell
XI_MIRROR[70] VDD Vbiasp VcascodeP[70] Iout Pmirror_StdCell
XI_MIRROR[69] VDD Vbiasp VcascodeP[69] Iout Pmirror_StdCell
XI_MIRROR[68] VDD Vbiasp VcascodeP[68] Iout Pmirror_StdCell
XI_MIRROR[67] VDD Vbiasp VcascodeP[67] Iout Pmirror_StdCell
XI_MIRROR[66] VDD Vbiasp VcascodeP[66] Iout Pmirror_StdCell
XI_MIRROR[65] VDD Vbiasp VcascodeP[65] Iout Pmirror_StdCell
XI_MIRROR[64] VDD Vbiasp VcascodeP[64] Iout Pmirror_StdCell
XI_MIRROR[63] VDD Vbiasp VcascodeP[63] Iout Pmirror_StdCell
XI_MIRROR[62] VDD Vbiasp VcascodeP[62] Iout Pmirror_StdCell
XI_MIRROR[61] VDD Vbiasp VcascodeP[61] Iout Pmirror_StdCell
XI_MIRROR[60] VDD Vbiasp VcascodeP[60] Iout Pmirror_StdCell
XI_MIRROR[59] VDD Vbiasp VcascodeP[59] Iout Pmirror_StdCell
XI_MIRROR[58] VDD Vbiasp VcascodeP[58] Iout Pmirror_StdCell
XI_MIRROR[57] VDD Vbiasp VcascodeP[57] Iout Pmirror_StdCell
XI_MIRROR[56] VDD Vbiasp VcascodeP[56] Iout Pmirror_StdCell
XI_MIRROR[55] VDD Vbiasp VcascodeP[55] Iout Pmirror_StdCell
XI_MIRROR[54] VDD Vbiasp VcascodeP[54] Iout Pmirror_StdCell
XI_MIRROR[53] VDD Vbiasp VcascodeP[53] Iout Pmirror_StdCell
XI_MIRROR[52] VDD Vbiasp VcascodeP[52] Iout Pmirror_StdCell
XI_MIRROR[51] VDD Vbiasp VcascodeP[51] Iout Pmirror_StdCell
XI_MIRROR[50] VDD Vbiasp VcascodeP[50] Iout Pmirror_StdCell
XI_MIRROR[49] VDD Vbiasp VcascodeP[49] Iout Pmirror_StdCell
XI_MIRROR[48] VDD Vbiasp VcascodeP[48] Iout Pmirror_StdCell
XI_MIRROR[47] VDD Vbiasp VcascodeP[47] Iout Pmirror_StdCell
XI_MIRROR[46] VDD Vbiasp VcascodeP[46] Iout Pmirror_StdCell
XI_MIRROR[45] VDD Vbiasp VcascodeP[45] Iout Pmirror_StdCell
XI_MIRROR[44] VDD Vbiasp VcascodeP[44] Iout Pmirror_StdCell
XI_MIRROR[43] VDD Vbiasp VcascodeP[43] Iout Pmirror_StdCell
XI_MIRROR[42] VDD Vbiasp VcascodeP[42] Iout Pmirror_StdCell
XI_MIRROR[41] VDD Vbiasp VcascodeP[41] Iout Pmirror_StdCell
XI_MIRROR[40] VDD Vbiasp VcascodeP[40] Iout Pmirror_StdCell
XI_MIRROR[39] VDD Vbiasp VcascodeP[39] Iout Pmirror_StdCell
XI_MIRROR[38] VDD Vbiasp VcascodeP[38] Iout Pmirror_StdCell
XI_MIRROR[37] VDD Vbiasp VcascodeP[37] Iout Pmirror_StdCell
XI_MIRROR[36] VDD Vbiasp VcascodeP[36] Iout Pmirror_StdCell
XI_MIRROR[35] VDD Vbiasp VcascodeP[35] Iout Pmirror_StdCell
XI_MIRROR[34] VDD Vbiasp VcascodeP[34] Iout Pmirror_StdCell
XI_MIRROR[33] VDD Vbiasp VcascodeP[33] Iout Pmirror_StdCell
XI_MIRROR[32] VDD Vbiasp VcascodeP[32] Iout Pmirror_StdCell
XI_MIRROR[31] VDD Vbiasp VcascodeP[31] Iout Pmirror_StdCell
XI_MIRROR[30] VDD Vbiasp VcascodeP[30] Iout Pmirror_StdCell
XI_MIRROR[29] VDD Vbiasp VcascodeP[29] Iout Pmirror_StdCell
XI_MIRROR[28] VDD Vbiasp VcascodeP[28] Iout Pmirror_StdCell
XI_MIRROR[27] VDD Vbiasp VcascodeP[27] Iout Pmirror_StdCell
XI_MIRROR[26] VDD Vbiasp VcascodeP[26] Iout Pmirror_StdCell
XI_MIRROR[25] VDD Vbiasp VcascodeP[25] Iout Pmirror_StdCell
XI_MIRROR[24] VDD Vbiasp VcascodeP[24] Iout Pmirror_StdCell
XI_MIRROR[23] VDD Vbiasp VcascodeP[23] Iout Pmirror_StdCell
XI_MIRROR[22] VDD Vbiasp VcascodeP[22] Iout Pmirror_StdCell
XI_MIRROR[21] VDD Vbiasp VcascodeP[21] Iout Pmirror_StdCell
XI_MIRROR[20] VDD Vbiasp VcascodeP[20] Iout Pmirror_StdCell
XI_MIRROR[19] VDD Vbiasp VcascodeP[19] Iout Pmirror_StdCell
XI_MIRROR[18] VDD Vbiasp VcascodeP[18] Iout Pmirror_StdCell
XI_MIRROR[17] VDD Vbiasp VcascodeP[17] Iout Pmirror_StdCell
XI_MIRROR[16] VDD Vbiasp VcascodeP[16] Iout Pmirror_StdCell
XI_MIRROR[15] VDD Vbiasp VcascodeP[15] Iout Pmirror_StdCell
XI_MIRROR[14] VDD Vbiasp VcascodeP[14] Iout Pmirror_StdCell
XI_MIRROR[13] VDD Vbiasp VcascodeP[13] Iout Pmirror_StdCell
XI_MIRROR[12] VDD Vbiasp VcascodeP[12] Iout Pmirror_StdCell
XI_MIRROR[11] VDD Vbiasp VcascodeP[11] Iout Pmirror_StdCell
XI_MIRROR[10] VDD Vbiasp VcascodeP[10] Iout Pmirror_StdCell
XI_MIRROR[9] VDD Vbiasp VcascodeP[9] Iout Pmirror_StdCell
XI_MIRROR[8] VDD Vbiasp VcascodeP[8] Iout Pmirror_StdCell
XI_MIRROR[7] VDD Vbiasp VcascodeP[7] Iout Pmirror_StdCell
XI_MIRROR[6] VDD Vbiasp VcascodeP[6] Iout Pmirror_StdCell
XI_MIRROR[5] VDD Vbiasp VcascodeP[5] Iout Pmirror_StdCell
XI_MIRROR[4] VDD Vbiasp VcascodeP[4] Iout Pmirror_StdCell
XI_MIRROR[3] VDD Vbiasp VcascodeP[3] Iout Pmirror_StdCell
XI_MIRROR[2] VDD Vbiasp VcascodeP[2] Iout Pmirror_StdCell
XI_MIRROR[1] VDD Vbiasp VcascodeP[1] Iout Pmirror_StdCell
XI_MIRROR[0] VDD Vbiasp VcascodeP[0] Iout Pmirror_StdCell
.ends


* expanding   symbol:  /home/user/PUDDING/schematic/DAC_SW.sym # of pins=5
** sym_path: schematic/DAC_SW.sym
** sch_path: schematic/DAC_SW.sch
.subckt DAC_SW VDD ON Pcascode_sw Pcascode ESDGND
*.ipin ON
*.ipin Pcascode
*.ipin ESDGND
*.ipin VDD
*.opin Pcascode_sw
XM1 VDD ON Pcascode_sw VDD sg13_lv_pmos w=0.5u l=0.13u ng=1 m=1 mm_ok=1
XM2 net1 ON VDD VDD sg13_lv_pmos w=0.15u l=0.13u ng=1 m=1 mm_ok=1
XM3 Pcascode net1 Pcascode_sw VDD sg13_lv_pmos w=0.5u l=0.13u ng=1 m=1 mm_ok=1
XM4 net1 ON ESDGND ESDGND sg13_lv_nmos w=0.15u l=0.13u ng=1 m=1 mm_ok=1
.ends


* expanding   symbol:  /home/user/PUDDING/schematic/Pmirror_StdCell.sym # of pins=4
** sym_path: /home/user/PUDDING/schematic/Pmirror_StdCell.sym
** sch_path: /home/user/PUDDING/schematic/Pmirror_StdCell.sch
.subckt Pmirror_StdCell VDD VbiasP VcascodeP Iout
*.ipin VcascodeP
*.ipin VbiasP
*.opin Iout
*.ipin VDD
XM2 net1 VbiasP VDD VDD sg13_lv_pmos w=0.15u l=0.13u ng=1 m=1 mm_ok=1
XM3 Iout VcascodeP net1 VDD sg13_lv_pmos w=0.15u l=0.13u ng=1 m=1 mm_ok=1
.ends

.end
